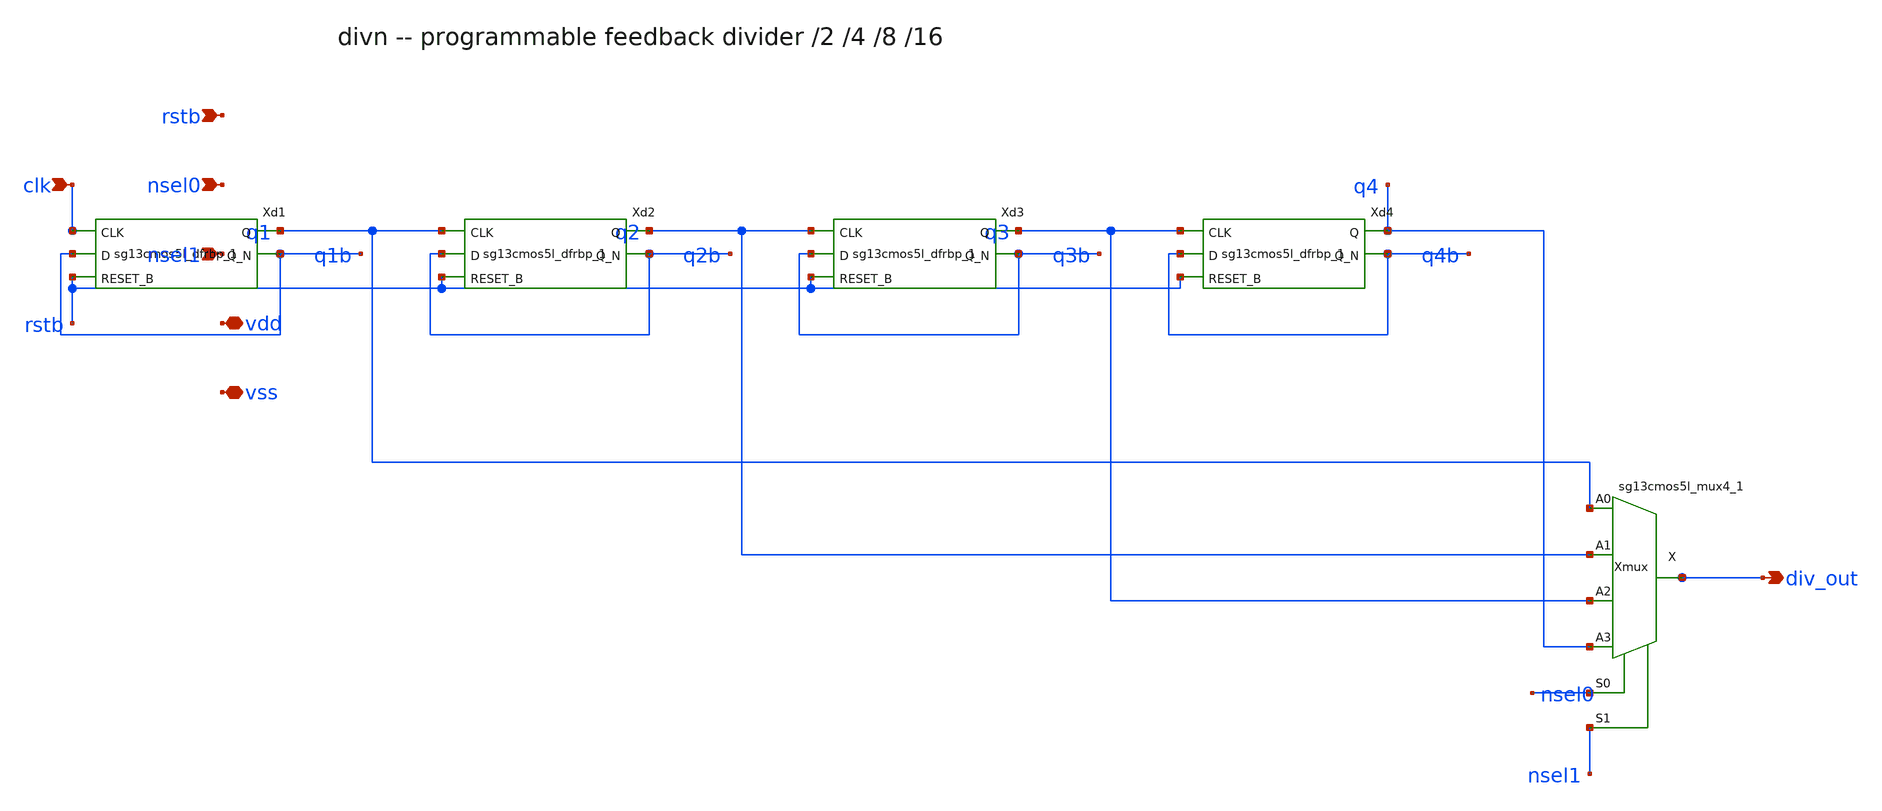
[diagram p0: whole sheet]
** sch_path: xschem/divn_wired.sch
**.subckt divn_wired clk rstb nsel0 nsel1 div_out vdd vss
*.ipin clk
*.ipin rstb
*.ipin nsel0
*.ipin nsel1
*.opin div_out
*.iopin vdd
*.iopin vss
Xd1 q1 q1b clk q1b rstb vdd vss sg13cmos5l_dfrbp_1
Xd2 q2 q2b q1 q2b rstb vdd vss sg13cmos5l_dfrbp_1
Xd3 q3 q3b q2 q3b rstb vdd vss sg13cmos5l_dfrbp_1
Xd4 q4 q4b q3 q4b rstb vdd vss sg13cmos5l_dfrbp_1
Xmux div_out q1 q2 q3 q4 nsel0 nsel1 vdd vss sg13cmos5l_mux4_1
**.ends
.end
